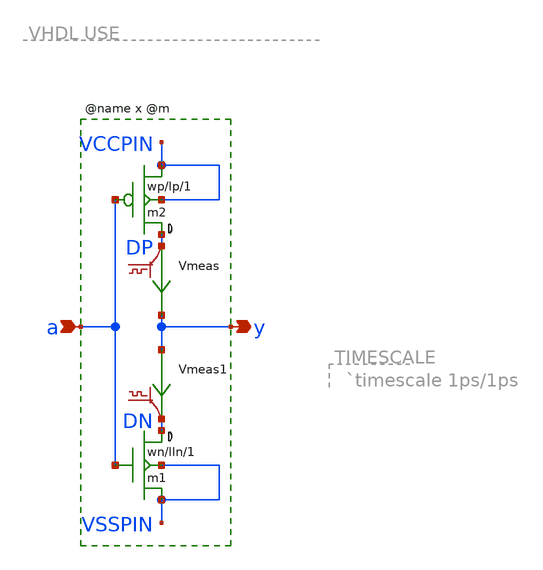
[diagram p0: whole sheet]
** sch_path: xschem_libs_newsym/rom8k/lvnot/schematic/lvnot.sch
* Copyright (C) 1998-2024 Stefan Frederik Schippers
* This program is free software; you can redistribute it and/or modify
* it under the terms of the GNU General Public License as published by
* the Free Software Foundation; either version 2 of the License, or
* (at your option) any later version.
* This program is distributed in the hope that it will be useful,
* but WITHOUT ANY WARRANTY; without even the implied warranty of
* MERCHANTABILITY or FITNESS FOR A PARTICULAR PURPOSE.  See the
* GNU General Public License for more details.
* You should have received a copy of the GNU General Public License
* along with this program; if not, write to the Free Software
**.subckt lvnot y a
*.opin y
*.ipin a
m2 DP a VCCPIN VCCPIN cmosp w=wp l=lp ad='wp *4.6u' as='wp *4.6u' pd='wp *2+9.2u' ps='wp *2+9.2u' m=1
m1 DN a VSSPIN VSSPIN cmosn w=wn l=lln ad='wn *4.3u' as='wn *4.3u' pd='wn *2+8.6u' ps='wn *2+8.6u' m=1
Vmeas DP y 0
.save i(vmeas)
Vmeas1 y DN 0
.save i(vmeas1)
.save v(dp)
.save v(dn)
**.ends
.end
